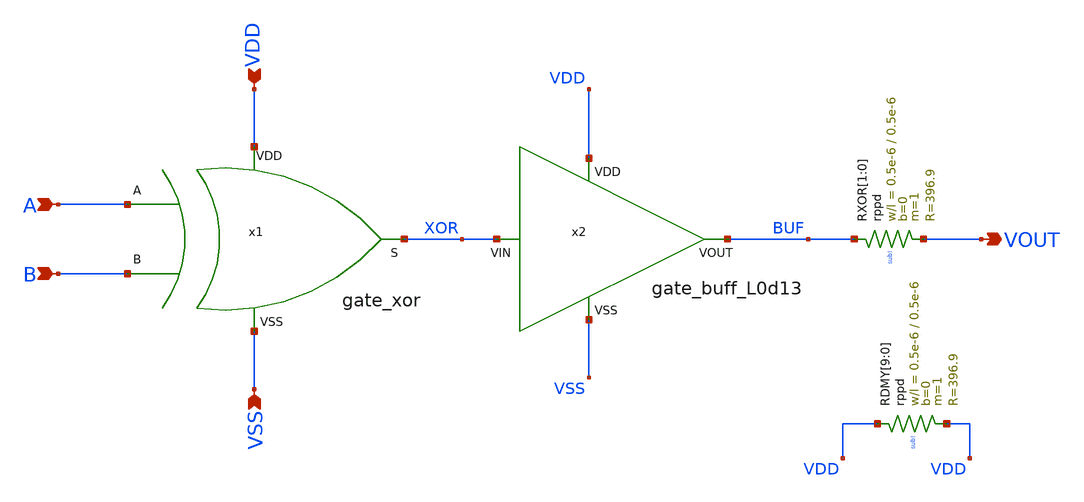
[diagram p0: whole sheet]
** sch_path: OSC9996-main/schematic/xschem/integrator_phasedetector.sch
**.subckt integrator_phasedetector A B VSS VDD VOUT
*.ipin A
*.ipin B
*.ipin VSS
*.ipin VDD
*.opin VOUT
x1 VDD XOR B A VSS gate_xor
x2 VDD XOR BUF VSS gate_buff_L0d13
XRXOR[1] BUF VOUT sub! rppd w=0.5e-6 l=0.5e-6 m=1 b=0 mm_ok=1
XRXOR[0] BUF VOUT sub! rppd w=0.5e-6 l=0.5e-6 m=1 b=0 mm_ok=1
XRDMY[9] VDD VDD sub! rppd w=0.5e-6 l=0.5e-6 m=1 b=0 mm_ok=1
XRDMY[8] VDD VDD sub! rppd w=0.5e-6 l=0.5e-6 m=1 b=0 mm_ok=1
XRDMY[7] VDD VDD sub! rppd w=0.5e-6 l=0.5e-6 m=1 b=0 mm_ok=1
XRDMY[6] VDD VDD sub! rppd w=0.5e-6 l=0.5e-6 m=1 b=0 mm_ok=1
XRDMY[5] VDD VDD sub! rppd w=0.5e-6 l=0.5e-6 m=1 b=0 mm_ok=1
XRDMY[4] VDD VDD sub! rppd w=0.5e-6 l=0.5e-6 m=1 b=0 mm_ok=1
XRDMY[3] VDD VDD sub! rppd w=0.5e-6 l=0.5e-6 m=1 b=0 mm_ok=1
XRDMY[2] VDD VDD sub! rppd w=0.5e-6 l=0.5e-6 m=1 b=0 mm_ok=1
XRDMY[1] VDD VDD sub! rppd w=0.5e-6 l=0.5e-6 m=1 b=0 mm_ok=1
XRDMY[0] VDD VDD sub! rppd w=0.5e-6 l=0.5e-6 m=1 b=0 mm_ok=1
**.ends
.end
